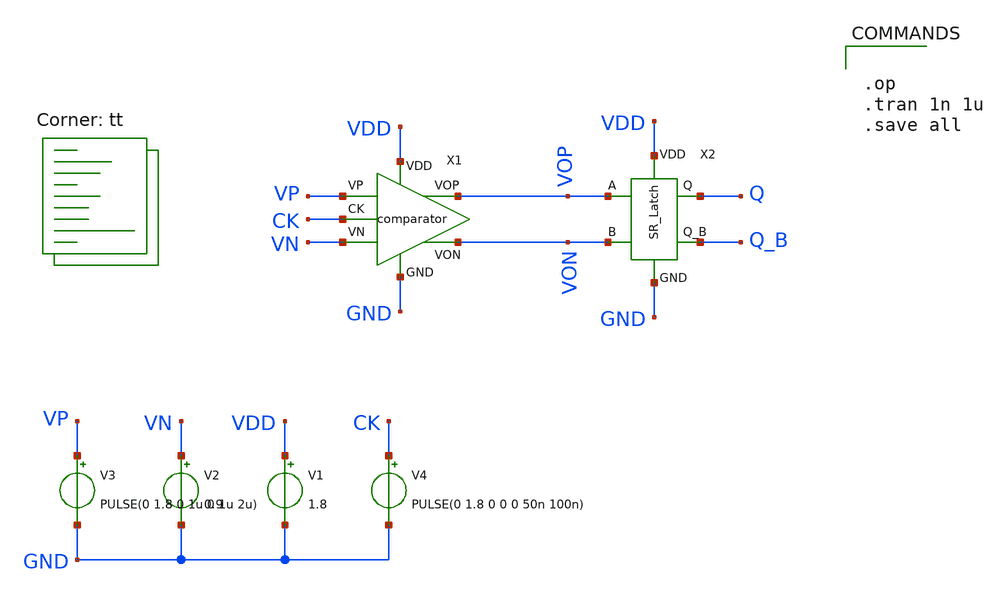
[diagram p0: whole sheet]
** sch_path: xschem/comparator_tb.sch
**.subckt comparator_tb
V1 VDD GND 1.8
V2 VN GND 0.9
V3 VP GND PULSE(0 1.8 0 1u 0 1u 2u)
V4 CK GND PULSE(0 1.8 0 0 0 50n 100n)
X1 VP VN GND VON VOP VDD CK comparator
X2 VOP VON GND VDD Q Q_B SR_Latch
**** begin user architecture code
.lib $::SKYWATER_MODELS/sky130.lib.spice tt


.op
.tran 1n 1u
.save all


**** end user architecture code
**.ends
.end
